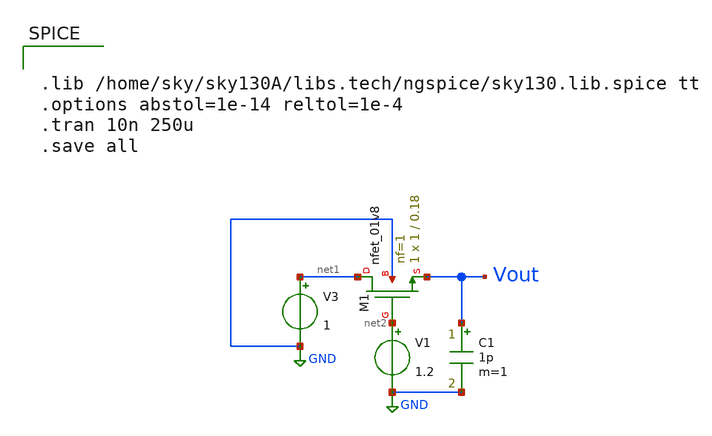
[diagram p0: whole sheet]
** sch_path: xschem/Switched_Caps/Characterizer.sch
**.subckt Characterizer
XM1 net1 net2 Vout GND sky130_fd_pr__nfet_01v8 L=0.18 W=1 nf=1 ad='int((nf+1)/2) * W/nf * 0.29' as='int((nf+2)/2) * W/nf * 0.29'
+ pd='2*int((nf+1)/2) * (W/nf + 0.29)' ps='2*int((nf+2)/2) * (W/nf + 0.29)' nrd='0.29 / W' nrs='0.29 / W'
+ sa=0 sb=0 sd=0 mult=1 m=1
V1 net2 GND 1.2
V3 net1 GND 1
C1 Vout GND 1p m=1
**** begin user architecture code


.lib /home/sky/sky130A/libs.tech/ngspice/sky130.lib.spice tt
.options abstol=1e-14 reltol=1e-4
.tran 10n 250u
.save all


**** end user architecture code
**.ends
.GLOBAL GND
.end
